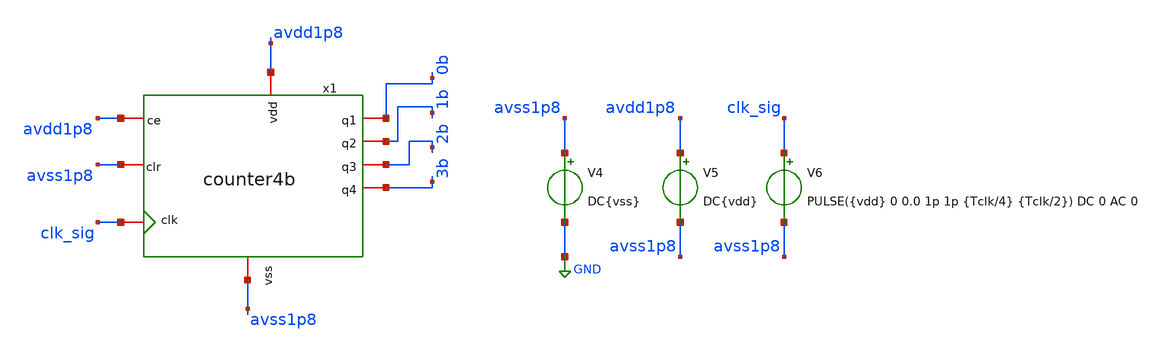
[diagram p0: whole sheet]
** sch_path: verification/testbenches/tb2_count4bits.sch
**.subckt tb2_count4bits
V4 avss1p8 GND DC{vss}
V5 avdd1p8 avss1p8 DC{vdd}
V6 clk_sig avss1p8 PULSE({vdd} 0 0.0 1p 1p {Tclk/4} {Tclk/2}) DC 0 AC 0
x1 avdd1p8 avss1p8 0b avdd1p8 avss1p8 clk_sig 1b 2b 3b counter4b
**** begin user architecture code


* Circuit Parameters
.param vdd = 1.2
.param vss = 0.0
.param Tclk = 10n
.options TEMP = 27.0
* Include Models - IHP SG13G2
.lib cornerMOSlv.lib mos_tt
* OP Parameters & Singals to save
.save all
*Simulations
.control
tran 0.01u 100n
setplot tran1
plot v(clk_sig) v(0b)+1.2 v(1b)+2.4 v(2b)+3.6 v(3b)+4.8
reset
dc V6 0 1.2 0.01
setplot dc
set filetype = ascii
write dcsweep.raw
.endc
.end


**** end user architecture code
**.ends

* expanding   symbol:  blocks/counter4b/schematic/counter4b.sym # of pins=9
** sym_path: design/top/schematic/counter4b.sym
** sch_path: design/top/schematic/counter4b.sch
.subckt counter4b vdd vss q1 ce clr clk q2 q3 q4
*.iopin ce
*.iopin q1
*.iopin q2
*.iopin q3
*.iopin q4
*.iopin clk
*.iopin clr
*.iopin vss
*.iopin vdd
x1 vdd ce net3 q1 vss andgate
x2 vdd q1 net1 ce vss xor
x3 q1 net8 net1 vss clk clr vdd dff
x4 vdd net3 net4 q2 vss andgate
x5 vdd q2 net2 net3 vss xor
x6 q2 net9 net2 vss clk clr vdd dff
x7 vdd net4 net7 q3 vss andgate
x8 vdd q3 net5 net4 vss xor
x9 q3 net10 net5 vss clk clr vdd dff
x11 vdd q4 net6 net7 vss xor
x12 q4 net11 net6 vss clk clr vdd dff
.ends


* expanding   symbol:  blocks/andgate/schematic/andgate.sym # of pins=5
** sym_path: design/blocks/andgate/schematic/andgate.sym
** sch_path: design/blocks/andgate/schematic/andgate.sch
.subckt andgate vdd a out b vss
*.iopin a
*.iopin b
*.iopin vss
*.iopin vdd
*.iopin out
x1 a b net1 vss vdd nand
x2 vdd out net1 vss inverter
.ends


* expanding   symbol:  blocks/xorgate/schematic/xor.sym # of pins=5
** sym_path: design/blocks/xorgate/schematic/xor.sym
** sch_path: design/blocks/xorgate/schematic/xor.sch
.subckt xor vdd a out b vss
*.iopin vss
*.iopin vdd
*.iopin a
*.iopin b
*.iopin out
XM1 net1 bb vdd vdd sg13_lv_pmos w=1.5u l=0.15u ng=1 m=1 mm_ok=1
XM2 out ab net2 vss sg13_lv_nmos w=1.5uu l=0.15u ng=1 m=1 mm_ok=1
XM3 net1 ab vdd vdd sg13_lv_pmos w=1.5u l=0.15u ng=1 m=1 mm_ok=1
XM4 out a net1 vdd sg13_lv_pmos w=1.5u l=0.15u ng=1 m=1 mm_ok=1
XM5 out b net1 vdd sg13_lv_pmos w=1.5u l=0.15u ng=1 m=1 mm_ok=1
XM6 out a net3 vss sg13_lv_nmos w=1.5u l=0.15u ng=1 m=1 mm_ok=1
x1 vdd ab a vss inverter
x2 vdd bb b vss inverter
XM7 net2 bb vss vss sg13_lv_nmos w=1.5u l=0.15u ng=1 m=1 mm_ok=1
XM8 net3 b vss vss sg13_lv_nmos w=1.5u l=0.15u ng=1 m=1 mm_ok=1
.ends


* expanding   symbol:  blocks/dff/schematic/dff.sym # of pins=7
** sym_path: design/blocks/dff/schematic/dff.sym
** sch_path: design/blocks/dff/schematic/dff.sch
.subckt dff q qb d vss clk clr vdd
*.iopin d
*.iopin clk
*.iopin clr
*.iopin q
*.iopin qb
*.iopin vdd
*.iopin vss
x1 clk vss net1 d vdd clkb transmissiongate
x2 vdd clr p1 net2 vss nor
x3 vdd clkb clk vss inverter
x4 clkb vss net1 net2 vdd clk transmissiongate
x5 clkb vss net3 p1 vdd clk transmissiongate
x6 clk vss qb net3 vdd clkb transmissiongate
x7 vdd clr net3 q vss nor
x8 vdd p1 net1 vss inverter
x9 vdd qb q vss inverter
.ends


* expanding   symbol:  blocks/nandgate/schematic/nand.sym # of pins=5
** sym_path: design/blocks/nandgate/schematic/nand.sym
** sch_path: design/blocks/nandgate/schematic/nand.sch
.subckt nand a b out vss vdd
*.iopin vdd
*.iopin a
*.iopin vss
*.iopin out
*.iopin b
XM1 out a vdd net2 sg13_lv_pmos w=0.15u l=0.13u ng=1 m=1 mm_ok=1
XM2 out a net1 net3 sg13_lv_nmos w=0.15u l=0.13u ng=1 m=1 mm_ok=1
XM3 net1 b net4 net5 sg13_lv_nmos w=0.15u l=0.13u ng=1 m=1 mm_ok=1
XM4 out b vdd net6 sg13_lv_pmos w=0.15u l=0.13u ng=1 m=1 mm_ok=1
.ends


* expanding   symbol:  blocks/inverter/schematic/inverter.sym # of pins=4
** sym_path: design/blocks/inverter/schematic/inverter.sym
** sch_path: design/blocks/inverter/schematic/inverter.sch
.subckt inverter vdd out in vss
*.iopin vdd
*.iopin out
*.iopin vss
*.iopin in
XM1 out in vss vss sg13_lv_nmos w=0.75u l=0.15u ng=1 m=1 mm_ok=1
XM2 out in vdd vdd sg13_lv_pmos w=1.5u l=0.15u ng=1 m=1 mm_ok=1
.ends


* expanding   symbol:  blocks/transmissiongate/schematic/transmissiongate.sym # of pins=6
** sym_path: design/blocks/transmissiongate/schematic/transmissiongate.sym
** sch_path: design/blocks/transmissiongate/schematic/transmissiongate.sch
.subckt transmissiongate clk vss out d vdd clkb
*.iopin out
*.iopin d
*.iopin clkb
*.iopin clk
*.iopin vdd
*.iopin vss
XM1 out clkb d vdd sg13_lv_pmos w=1.5u l=0.15u ng=1 m=1 mm_ok=1
XM0 d clk out vss sg13_lv_nmos w=0.75u l=0.15u ng=1 m=1 mm_ok=1
.ends


* expanding   symbol:  blocks/norgate/schematic/nor.sym # of pins=5
** sym_path: design/blocks/norgate/schematic/nor.sym
** sch_path: design/blocks/norgate/schematic/nor.sch
.subckt nor vdd a b out vss
*.iopin vdd
*.iopin a
*.iopin vss
*.iopin out
*.iopin b
XM1 net1 a vdd vdd sg13_lv_pmos w=3.0u l=0.15u ng=1 m=1 mm_ok=1
XM2 out b vss vss sg13_lv_nmos w=0.75u l=0.15u ng=1 m=1 mm_ok=1
XM3 out a vss vss sg13_lv_nmos w=0.75u l=0.15u ng=1 m=1 mm_ok=1
XM4 out b net1 vdd sg13_lv_pmos w=3.0u l=0.15u ng=1 m=1 mm_ok=1
.ends

.GLOBAL GND
.end
